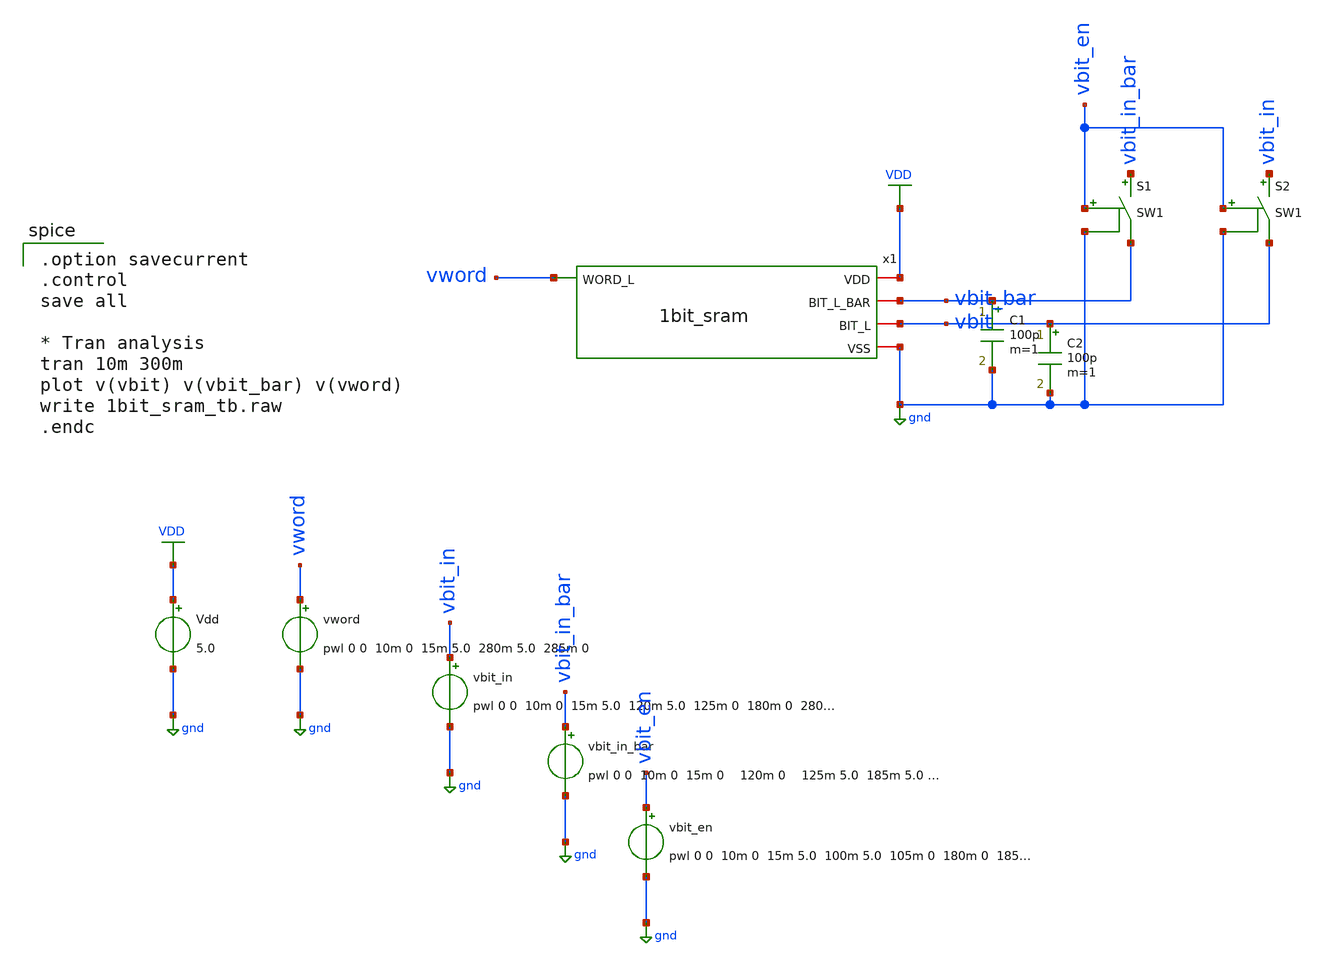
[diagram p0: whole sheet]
** sch_path: member_project/SRAM/noritsuna/1bit_sram_tb.sch
**.subckt 1bit_sram_tb
x1 vword VDD vbit_bar vbit gnd 1bit_sram
Vdd VDD gnd 5.0
vword vword gnd pwl 0 0 10m 0 15m 5.0 280m 5.0 285m 0
vbit_in vbit_in gnd pwl 0 0 10m 0 15m 5.0 120m 5.0 125m 0 180m 0 280m 0
vbit_in_bar vbit_in_bar gnd pwl 0 0 10m 0 15m 0 120m 0 125m 5.0 185m 5.0 280m 5.0
vbit_en vbit_en gnd pwl 0 0 10m 0 15m 5.0 100m 5.0 105m 0 180m 0 185m 5.0 250m 5.0 255m 0
S1 vbit_in_bar vbit_bar vbit_en gnd SW1
S2 vbit_in vbit vbit_en gnd SW1
C1 vbit_bar gnd 100p m=1
C2 vbit gnd 100p m=1
**** begin user architecture code
 .include $::LIB/ip62_models

.option savecurrent
.control
save all

* Tran analysis
tran 10m 300m
plot v(vbit) v(vbit_bar) v(vword)
write 1bit_sram_tb.raw
.endc

**** end user architecture code
**.ends

* expanding   symbol:  1bit_sram.sym # of pins=5
** sym_path: member_project/SRAM/noritsuna/1bit_sram.sym
** sch_path: member_project/SRAM/noritsuna/1bit_sram.sch
.subckt 1bit_sram WORD_L VDD BIT_L_BAR BIT_L VSS
*.iopin VDD
*.iopin VSS
*.iopin BIT_L_BAR
*.iopin BIT_L
*.ipin WORD_L
XXM1 net2 net1 VDD VDD PMOS w=24u l=4.2u nrd=0 nrs=0 m=12
XXM2 net2 net1 VSS VSS NMOS w=24u l=4.2u nrd=0 nrs=0 m=40
XXM3 net1 net2 VDD VDD PMOS w=24u l=4.2u nrd=0 nrs=0 m=12
XXM4 net1 net2 VSS VSS NMOS w=24u l=4.2u nrd=0 nrs=0 m=40
XXM5 BIT_L_BAR WORD_L net1 VSS NMOS w=24u l=4.2u nrd=0 nrs=0 m=20
XXM6 BIT_L WORD_L net2 VSS NMOS w=24u l=4.2u nrd=0 nrs=0 m=20
.ends

.GLOBAL VDD
.GLOBAL gnd
**** begin user architecture code
.MODEL SW1 SW  VT=2.5 VH=0.2  RON=1 ROFF=100Meg
**** end user architecture code
.end
